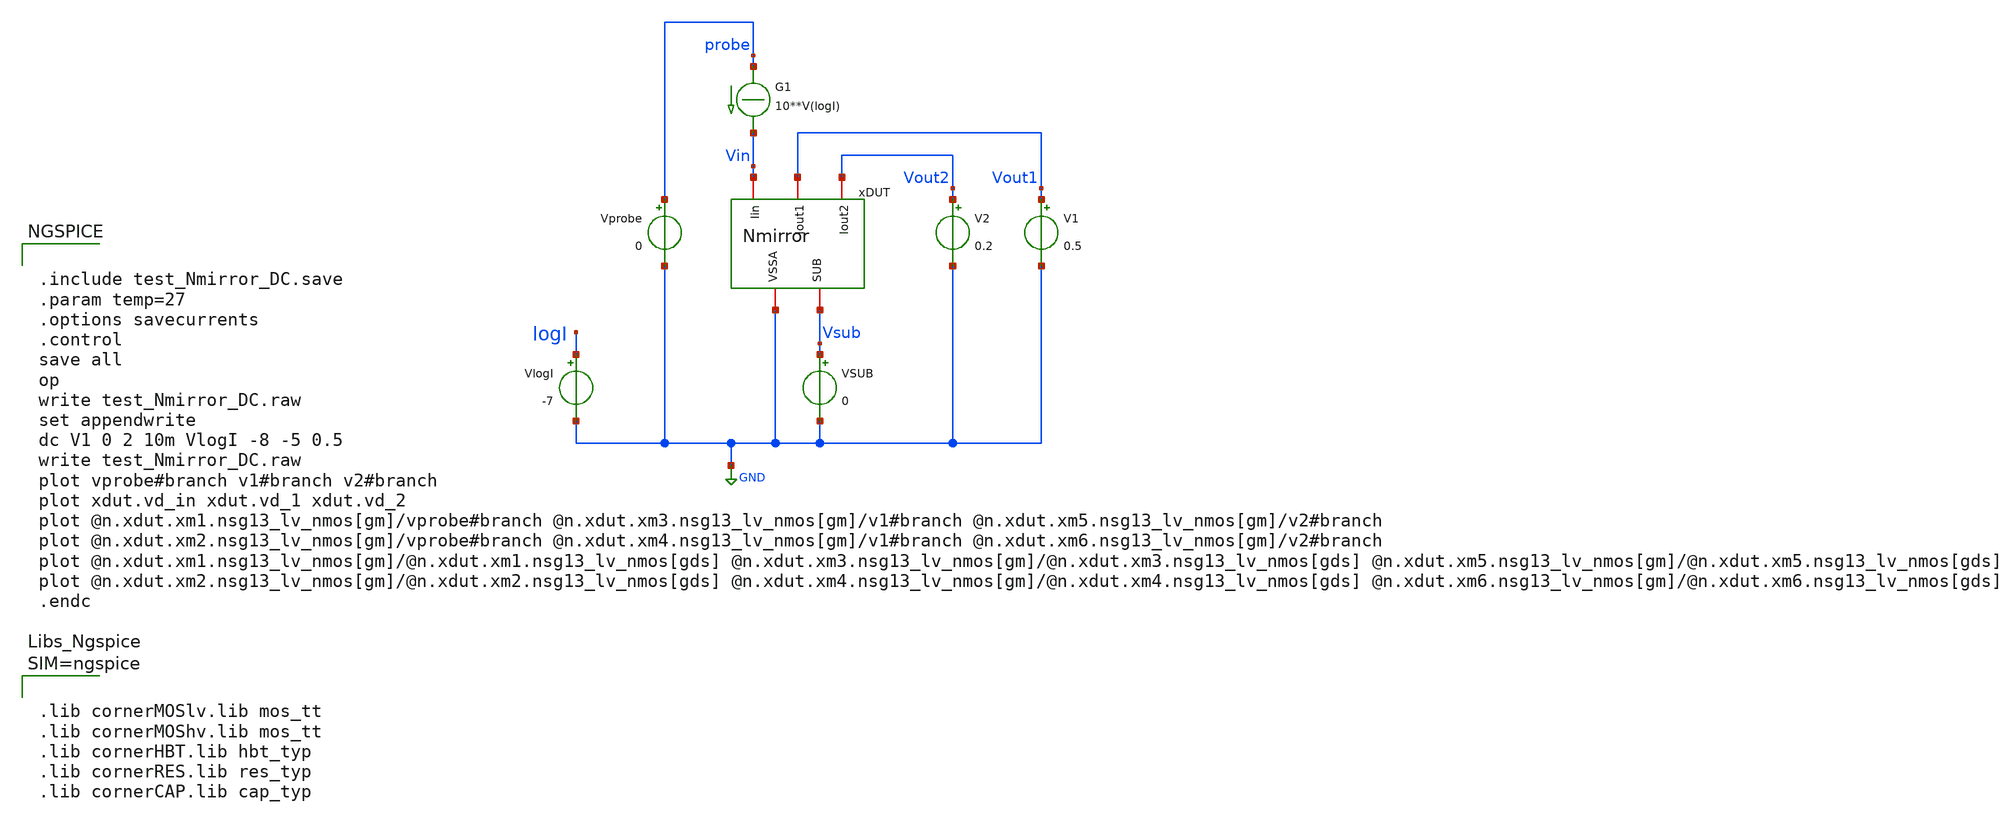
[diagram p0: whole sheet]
** sch_path: xschem/test_Nmirror_DC.sch
**.subckt test_Nmirror_DC
xDUT Vout2 Vin Vout1 GND Vsub Nmirror
V1 Vout1 GND 0.5
.save i(v1)
V2 Vout2 GND 0.2
.save i(v2)
VSUB Vsub GND 0
.save i(vsub)
Vprobe probe GND 0
.save i(vprobe)
G1 probe Vin CUR=' 10**V(logI) '
VlogI logI GND -7
.save i(vlogi)
**** begin user architecture code


.include test_Nmirror_DC.save
.param temp=27
.options savecurrents
.control
save all
op
write test_Nmirror_DC.raw
set appendwrite
dc V1 0 2 10m VlogI -8 -5 0.5
write test_Nmirror_DC.raw
plot vprobe#branch v1#branch v2#branch
plot xdut.vd_in xdut.vd_1 xdut.vd_2
plot @n.xdut.xm1.nsg13_lv_nmos[gm]/vprobe#branch @n.xdut.xm3.nsg13_lv_nmos[gm]/v1#branch
+ @n.xdut.xm5.nsg13_lv_nmos[gm]/v2#branch
plot @n.xdut.xm2.nsg13_lv_nmos[gm]/vprobe#branch @n.xdut.xm4.nsg13_lv_nmos[gm]/v1#branch
+ @n.xdut.xm6.nsg13_lv_nmos[gm]/v2#branch
plot @n.xdut.xm1.nsg13_lv_nmos[gm]/@n.xdut.xm1.nsg13_lv_nmos[gds]
+ @n.xdut.xm3.nsg13_lv_nmos[gm]/@n.xdut.xm3.nsg13_lv_nmos[gds] @n.xdut.xm5.nsg13_lv_nmos[gm]/@n.xdut.xm5.nsg13_lv_nmos[gds]
plot @n.xdut.xm2.nsg13_lv_nmos[gm]/@n.xdut.xm2.nsg13_lv_nmos[gds]
+ @n.xdut.xm4.nsg13_lv_nmos[gm]/@n.xdut.xm4.nsg13_lv_nmos[gds] @n.xdut.xm6.nsg13_lv_nmos[gm]/@n.xdut.xm6.nsg13_lv_nmos[gds]
.endc





.lib cornerMOSlv.lib mos_tt
.lib cornerMOShv.lib mos_tt
.lib cornerHBT.lib hbt_typ
.lib cornerRES.lib res_typ
.lib cornerCAP.lib cap_typ



**** end user architecture code
**.ends

* expanding   symbol:  Nmirror.sym # of pins=5
** sym_path: xschem/Nmirror.sym
** sch_path: xschem/Nmirror.sch
.subckt Nmirror Iout2 Iin Iout1 VSSA SUB
*.iopin VSSA
*.iopin SUB
*.iopin Iin
*.iopin Iout1
*.iopin Iout2
XM1 vd_in Iin VSSA SUB sg13_lv_nmos w=0.4u l=4.0u ng=1 m=1 mm_ok=1
XM3 vd_1 Iin VSSA SUB sg13_lv_nmos w=0.4u l=4.0u ng=1 m=1 mm_ok=1
XM2 Iin Iin vd_in SUB sg13_lv_nmos w=4u l=0.26u ng=1 m=1 mm_ok=1
XM4 Iout1 Iin vd_1 SUB sg13_lv_nmos w=4u l=0.26u ng=1 m=1 mm_ok=1
XM5 vd_2 Iin VSSA SUB sg13_lv_nmos w=0.4u l=4.0u ng=1 m=1 mm_ok=1
XM6 Iout2 Iin vd_2 SUB sg13_lv_nmos w=4u l=0.26u ng=1 m=1 mm_ok=1
.ends

.GLOBAL GND
.end
